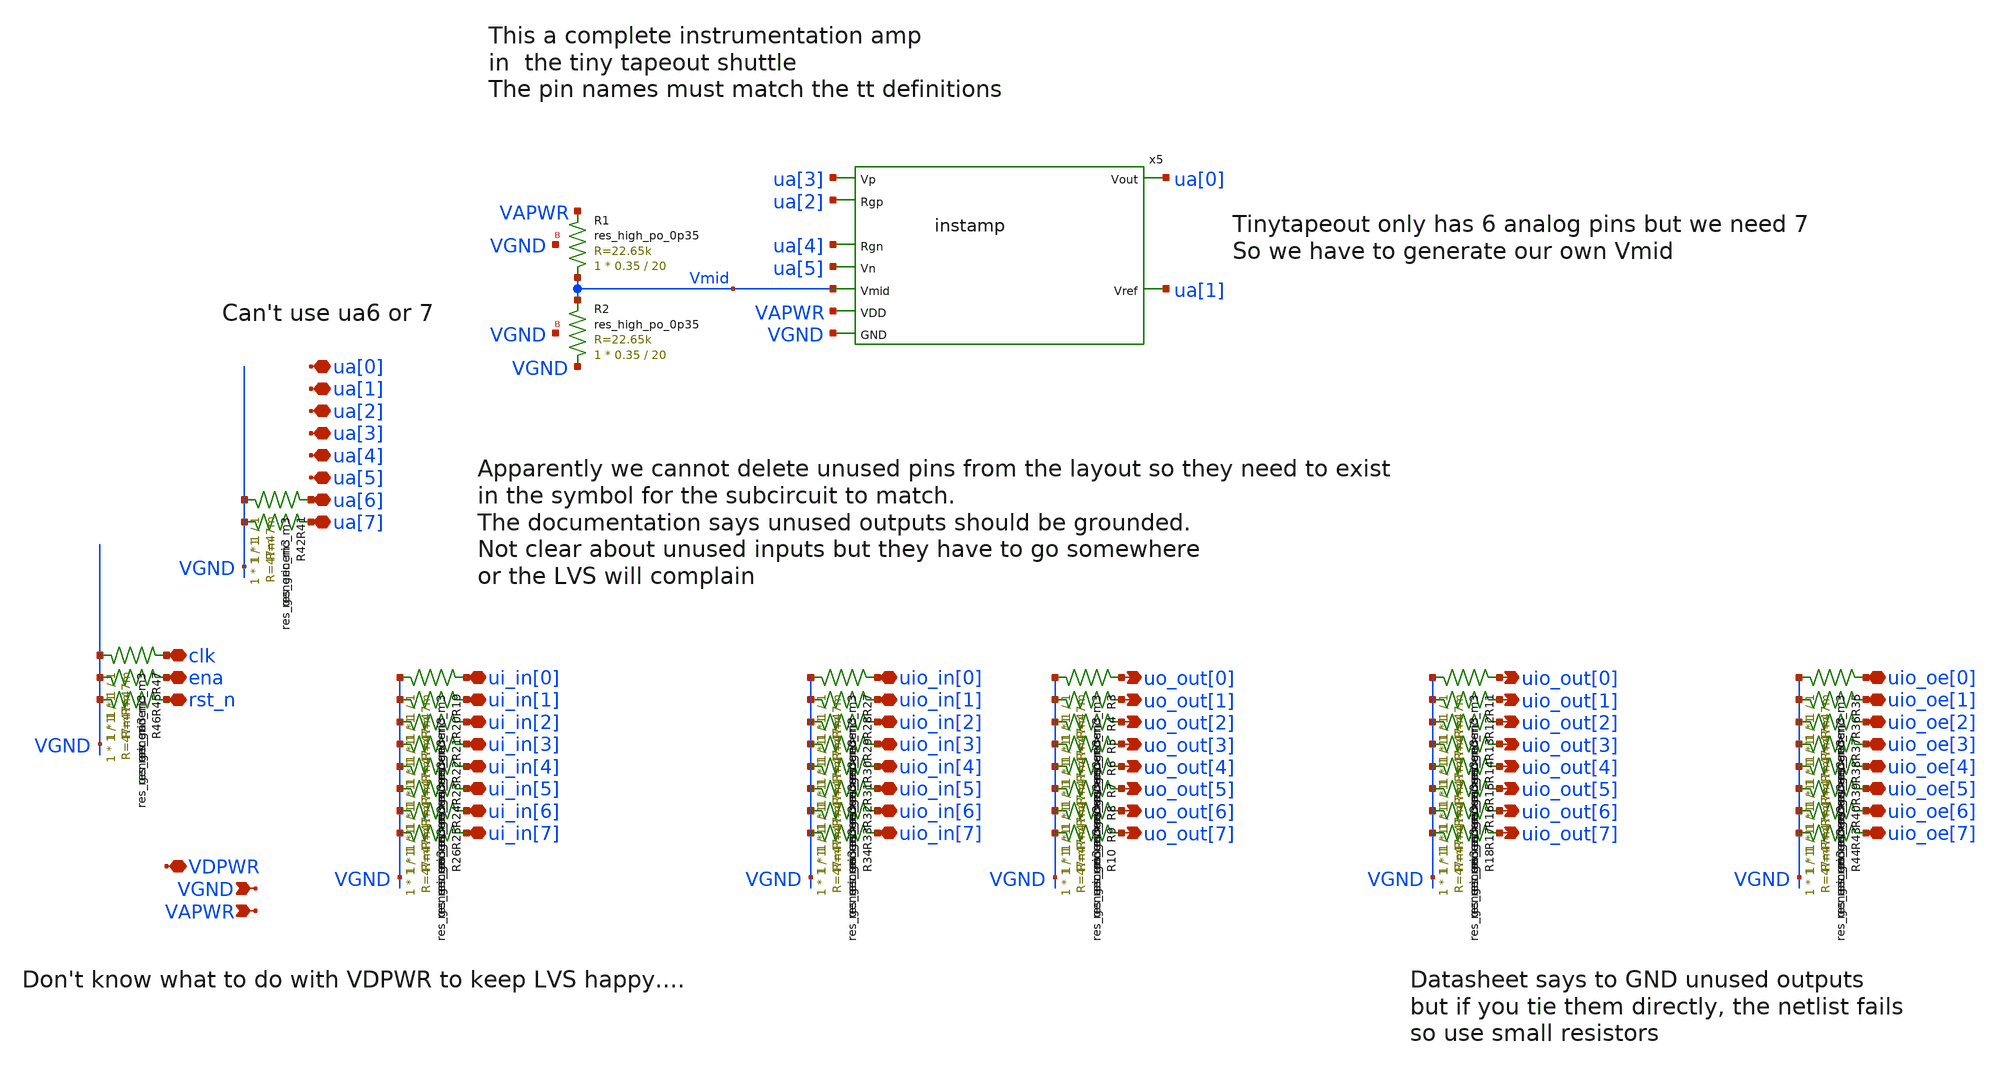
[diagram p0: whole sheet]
** sch_path: xschem/tt_um_jonathanwest3_instamp_sp2026.sch
* Copyright 2021 Stefan Frederik Schippers
* Licensed under the Apache License, Version 2.0 (the "License");
* you may not use this file except in compliance with the License.
* You may obtain a copy of the License at
* https://www.apache.org/licenses/LICENSE-2.0
* Unless required by applicable law or agreed to in writing, software
* distributed under the License is distributed on an "AS IS" BASIS,
* WITHOUT WARRANTIES OR CONDITIONS OF ANY KIND, either express or implied.
* See the License for the specific language governing permissions and
* limitations under the License.
**.subckt tt_um_jonathanwest3_instamp_sp2026 VGND VAPWR uo_out[0] uo_out[1] uo_out[2] uo_out[3]
*+ uo_out[4] uo_out[5] uo_out[6] uo_out[7] uio_out[0] uio_out[1] uio_out[2] uio_out[3] uio_out[4] uio_out[5]
*+ uio_out[6] uio_out[7] ui_in[7] clk ena rst_n VDPWR uio_oe[0] uio_in[0] ui_in[6] ui_in[5] ui_in[4] ui_in[3]
*+ ui_in[2] ui_in[1] ui_in[0] ua[0] ua[1] ua[2] ua[3] ua[4] ua[5] ua[6] ua[7] uio_oe[1] uio_oe[2] uio_oe[3]
*+ uio_oe[4] uio_oe[5] uio_oe[6] uio_oe[7] uio_in[1] uio_in[2] uio_in[3] uio_in[4] uio_in[5] uio_in[6] uio_in[7]
*.ipin VGND
*.ipin VAPWR
*.opin uo_out[0]
*.opin uo_out[1]
*.opin uo_out[2]
*.opin uo_out[3]
*.opin uo_out[4]
*.opin uo_out[5]
*.opin uo_out[6]
*.opin uo_out[7]
*.opin uio_out[0]
*.opin uio_out[1]
*.opin uio_out[2]
*.opin uio_out[3]
*.opin uio_out[4]
*.opin uio_out[5]
*.opin uio_out[6]
*.opin uio_out[7]
*.iopin ui_in[7]
*.iopin clk
*.iopin ena
*.iopin rst_n
*.iopin VDPWR
*.iopin uio_oe[0]
*.iopin uio_in[0]
*.iopin ui_in[6]
*.iopin ui_in[5]
*.iopin ui_in[4]
*.iopin ui_in[3]
*.iopin ui_in[2]
*.iopin ui_in[1]
*.iopin ui_in[0]
*.iopin ua[0]
*.iopin ua[1]
*.iopin ua[2]
*.iopin ua[3]
*.iopin ua[4]
*.iopin ua[5]
*.iopin ua[6]
*.iopin ua[7]
*.iopin uio_oe[1]
*.iopin uio_oe[2]
*.iopin uio_oe[3]
*.iopin uio_oe[4]
*.iopin uio_oe[5]
*.iopin uio_oe[6]
*.iopin uio_oe[7]
*.iopin uio_in[1]
*.iopin uio_in[2]
*.iopin uio_in[3]
*.iopin uio_in[4]
*.iopin uio_in[5]
*.iopin uio_in[6]
*.iopin uio_in[7]
x5 ua[5] ua[4] ua[3] ua[2] Vmid ua[0] ua[1] VAPWR VGND instamp
XR1 Vmid VAPWR VGND sky130_fd_pr__res_high_po_0p35 L=20 mult=1 m=1
XR2 VGND Vmid VGND sky130_fd_pr__res_high_po_0p35 L=20 mult=1 m=1
R3 VGND uo_out[0] sky130_fd_pr__res_generic_m3 W=1 L=1 m=1
R4 VGND uo_out[1] sky130_fd_pr__res_generic_m3 W=1 L=1 m=1
R5 VGND uo_out[2] sky130_fd_pr__res_generic_m3 W=1 L=1 m=1
R6 VGND uo_out[3] sky130_fd_pr__res_generic_m3 W=1 L=1 m=1
R7 VGND uo_out[4] sky130_fd_pr__res_generic_m3 W=1 L=1 m=1
R8 VGND uo_out[5] sky130_fd_pr__res_generic_m3 W=1 L=1 m=1
R9 VGND uo_out[6] sky130_fd_pr__res_generic_m3 W=1 L=1 m=1
R10 VGND uo_out[7] sky130_fd_pr__res_generic_m3 W=1 L=1 m=1
R11 VGND uio_out[0] sky130_fd_pr__res_generic_m3 W=1 L=1 m=1
R12 VGND uio_out[1] sky130_fd_pr__res_generic_m3 W=1 L=1 m=1
R13 VGND uio_out[2] sky130_fd_pr__res_generic_m3 W=1 L=1 m=1
R14 VGND uio_out[3] sky130_fd_pr__res_generic_m3 W=1 L=1 m=1
R15 VGND uio_out[4] sky130_fd_pr__res_generic_m3 W=1 L=1 m=1
R16 VGND uio_out[5] sky130_fd_pr__res_generic_m3 W=1 L=1 m=1
R17 VGND uio_out[6] sky130_fd_pr__res_generic_m3 W=1 L=1 m=1
R18 VGND uio_out[7] sky130_fd_pr__res_generic_m3 W=1 L=1 m=1
R19 VGND ui_in[0] sky130_fd_pr__res_generic_m3 W=1 L=1 m=1
R20 VGND ui_in[1] sky130_fd_pr__res_generic_m3 W=1 L=1 m=1
R21 VGND ui_in[2] sky130_fd_pr__res_generic_m3 W=1 L=1 m=1
R22 VGND ui_in[3] sky130_fd_pr__res_generic_m3 W=1 L=1 m=1
R23 VGND ui_in[4] sky130_fd_pr__res_generic_m3 W=1 L=1 m=1
R24 VGND ui_in[5] sky130_fd_pr__res_generic_m3 W=1 L=1 m=1
R25 VGND ui_in[6] sky130_fd_pr__res_generic_m3 W=1 L=1 m=1
R26 VGND ui_in[7] sky130_fd_pr__res_generic_m3 W=1 L=1 m=1
R27 VGND uio_in[0] sky130_fd_pr__res_generic_m3 W=1 L=1 m=1
R28 VGND uio_in[1] sky130_fd_pr__res_generic_m3 W=1 L=1 m=1
R29 VGND uio_in[2] sky130_fd_pr__res_generic_m3 W=1 L=1 m=1
R30 VGND uio_in[3] sky130_fd_pr__res_generic_m3 W=1 L=1 m=1
R31 VGND uio_in[4] sky130_fd_pr__res_generic_m3 W=1 L=1 m=1
R32 VGND uio_in[5] sky130_fd_pr__res_generic_m3 W=1 L=1 m=1
R33 VGND uio_in[6] sky130_fd_pr__res_generic_m3 W=1 L=1 m=1
R34 VGND uio_in[7] sky130_fd_pr__res_generic_m3 W=1 L=1 m=1
R41 VGND ua[6] sky130_fd_pr__res_generic_m3 W=1 L=1 m=1
R42 VGND ua[7] sky130_fd_pr__res_generic_m3 W=1 L=1 m=1
R35 VGND uio_oe[0] sky130_fd_pr__res_generic_m3 W=1 L=1 m=1
R36 VGND uio_oe[1] sky130_fd_pr__res_generic_m3 W=1 L=1 m=1
R37 VGND uio_oe[2] sky130_fd_pr__res_generic_m3 W=1 L=1 m=1
R38 VGND uio_oe[3] sky130_fd_pr__res_generic_m3 W=1 L=1 m=1
R39 VGND uio_oe[4] sky130_fd_pr__res_generic_m3 W=1 L=1 m=1
R40 VGND uio_oe[5] sky130_fd_pr__res_generic_m3 W=1 L=1 m=1
R43 VGND uio_oe[6] sky130_fd_pr__res_generic_m3 W=1 L=1 m=1
R44 VGND uio_oe[7] sky130_fd_pr__res_generic_m3 W=1 L=1 m=1
R45 VGND ena sky130_fd_pr__res_generic_m3 W=1 L=1 m=1
R46 VGND rst_n sky130_fd_pr__res_generic_m3 W=1 L=1 m=1
R47 VGND clk sky130_fd_pr__res_generic_m3 W=1 L=1 m=1
**.ends
.end
